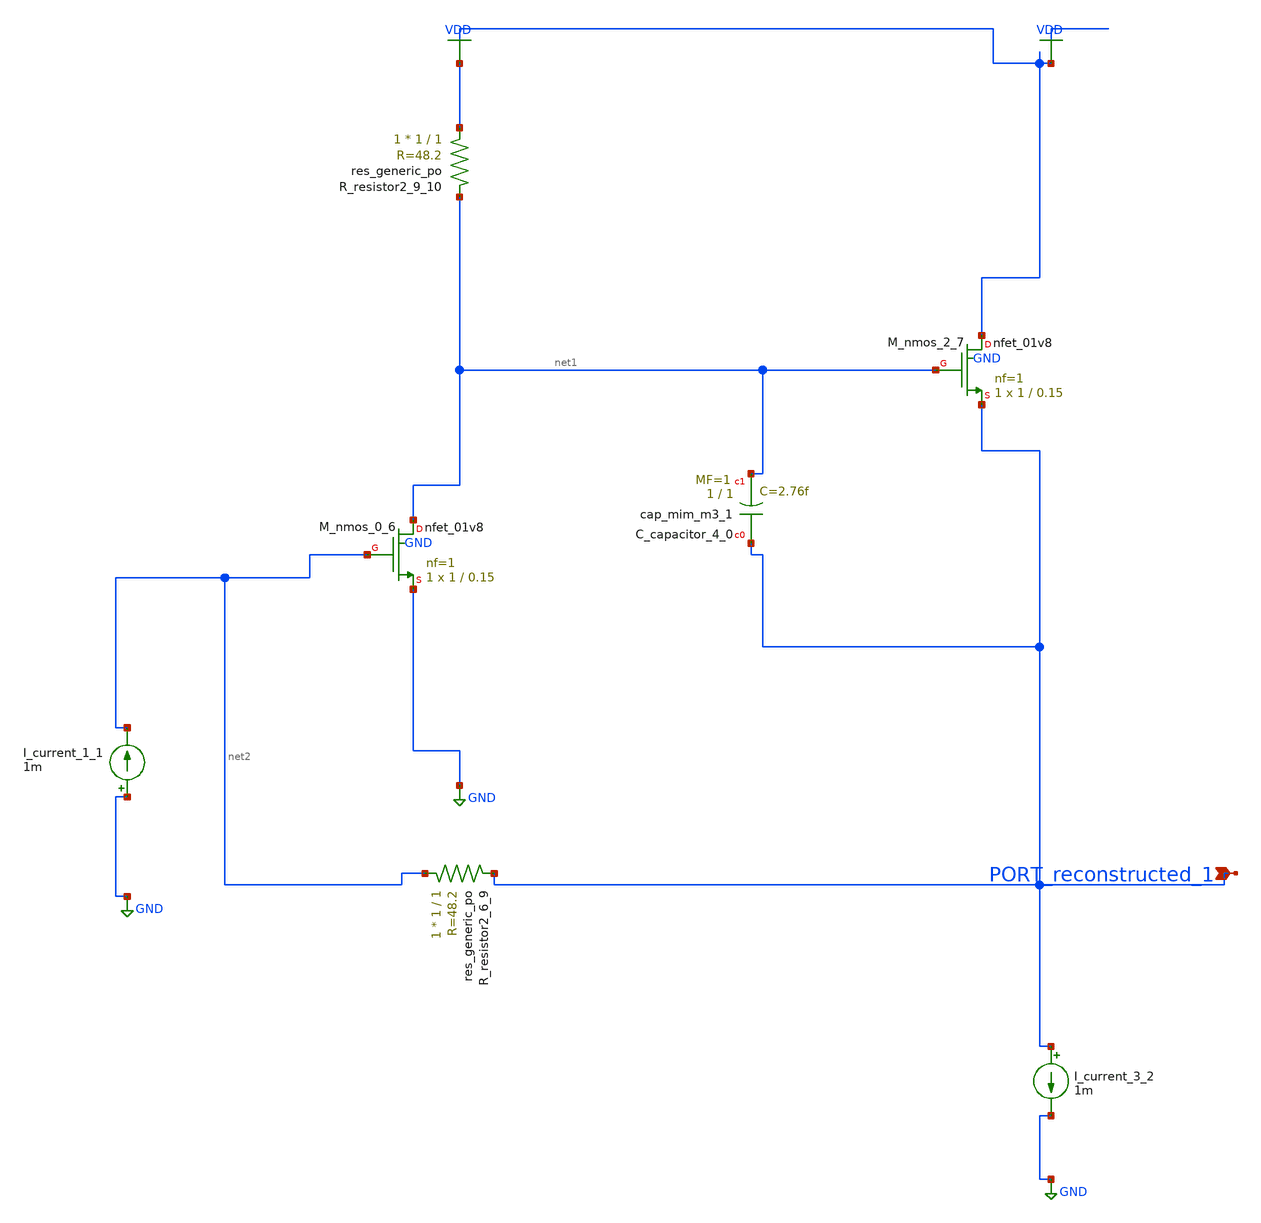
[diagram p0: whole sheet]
** sch_path: schematics/AMSNet/570.sch
**.subckt 570 PORT_reconstructed_1
*.ipin PORT_reconstructed_1
XC_capacitor_4_0 PORT_reconstructed_1 net1 sky130_fd_pr__cap_mim_m3_1 W=1 L=1 MF=1 m=1
I_current_1_1 GND net2 1m
I_current_3_2 PORT_reconstructed_1 GND 1m
XM_nmos_0_6 net1 net2 GND GND sky130_fd_pr__nfet_01v8 L=0.15 W=1 nf=1 ad='int((1 + 1)/2) * 1 / 1 * 0.29'
+ as='int((1 + 2)/2) * 1 / 1 * 0.29' pd='2*int((1 + 1)/2) * (1 / 1 + 0.29)' ps='2*int((1 + 2)/2) * (1 / 1 + 0.29)'
+ nrd='0.29 / 1 ' nrs='0.29 / 1 ' sa=0 sb=0 sd=0 mult=1 m=1
XM_nmos_2_7 VDD net1 PORT_reconstructed_1 GND sky130_fd_pr__nfet_01v8 L=0.15 W=1 nf=1 ad='int((1 + 1)/2) * 1 / 1 * 0.29'
+ as='int((1 + 2)/2) * 1 / 1 * 0.29' pd='2*int((1 + 1)/2) * (1 / 1 + 0.29)' ps='2*int((1 + 2)/2) * (1 / 1 + 0.29)'
+ nrd='0.29 / 1 ' nrs='0.29 / 1 ' sa=0 sb=0 sd=0 mult=1 m=1
XR_resistor2_6_9 net2 PORT_reconstructed_1 sky130_fd_pr__res_generic_po W=1 L=1 m=1
XR_resistor2_9_10 VDD net1 sky130_fd_pr__res_generic_po W=1 L=1 m=1
**.ends
.GLOBAL GND
.GLOBAL VDD
.end
